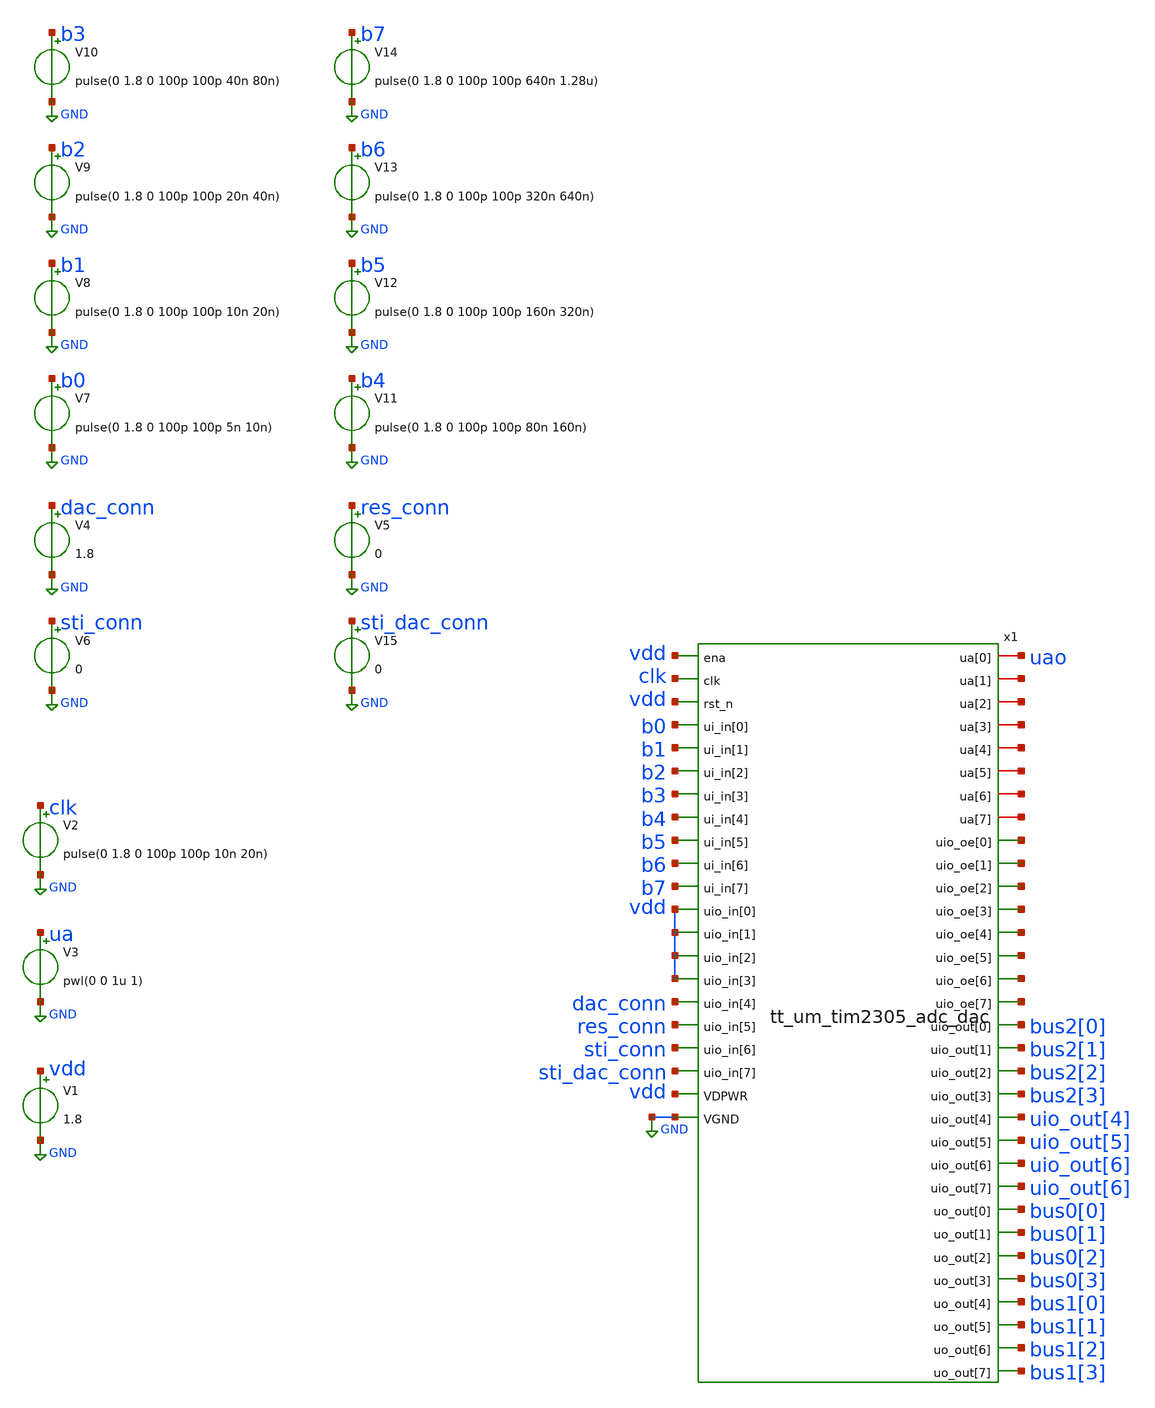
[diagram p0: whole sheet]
** sch_path: xschem/top_tb.sch
**.subckt top_tb
V1 vdd GND 1.8
V3 ua GND pwl(0 0 1u 1)
V2 clk GND pulse(0 1.8 0 100p 100p 10n 20n)
x1 uao net1 net2 net3 net4 net5 net6 vdd net7 clk vdd net8 b0 net9 b1 net10 net11 b2 b3 net12 b4
+ net13 b5 net14 net15 b6 b7 bus2[0] vdd bus2[1] vdd bus2[2] vdd bus2[3] uio_out[4] vdd uio_out[5] dac_conn
+ uio_out[6] res_conn sti_conn uio_out[6] sti_dac_conn bus0[0] vdd bus0[1] GND bus0[2] bus0[3] bus1[0] bus1[1]
+ bus1[2] bus1[3] tt_um_tim2305_adc_dac
V7 b0 GND pulse(0 1.8 0 100p 100p 5n 10n)
V8 b1 GND pulse(0 1.8 0 100p 100p 10n 20n)
V9 b2 GND pulse(0 1.8 0 100p 100p 20n 40n)
V10 b3 GND pulse(0 1.8 0 100p 100p 40n 80n)
V11 b4 GND pulse(0 1.8 0 100p 100p 80n 160n)
V12 b5 GND pulse(0 1.8 0 100p 100p 160n 320n)
V13 b6 GND pulse(0 1.8 0 100p 100p 320n 640n)
V14 b7 GND pulse(0 1.8 0 100p 100p 640n 1.28u)
V4 dac_conn GND 1.8
V5 res_conn GND 0
V6 sti_conn GND 0
V15 sti_dac_conn GND 0
**** begin user architecture code


.tran 100p 1.28u
.save all
.lib /home/ttuser/pdk/sky130A/libs.tech/ngspice/sky130.lib.spice tt
.include /home/ttuser/Documents/github_project/adc_dac2/mag/tt_um_tim2305_adc_dac.spice


**** end user architecture code
**.ends
.GLOBAL GND
.end
